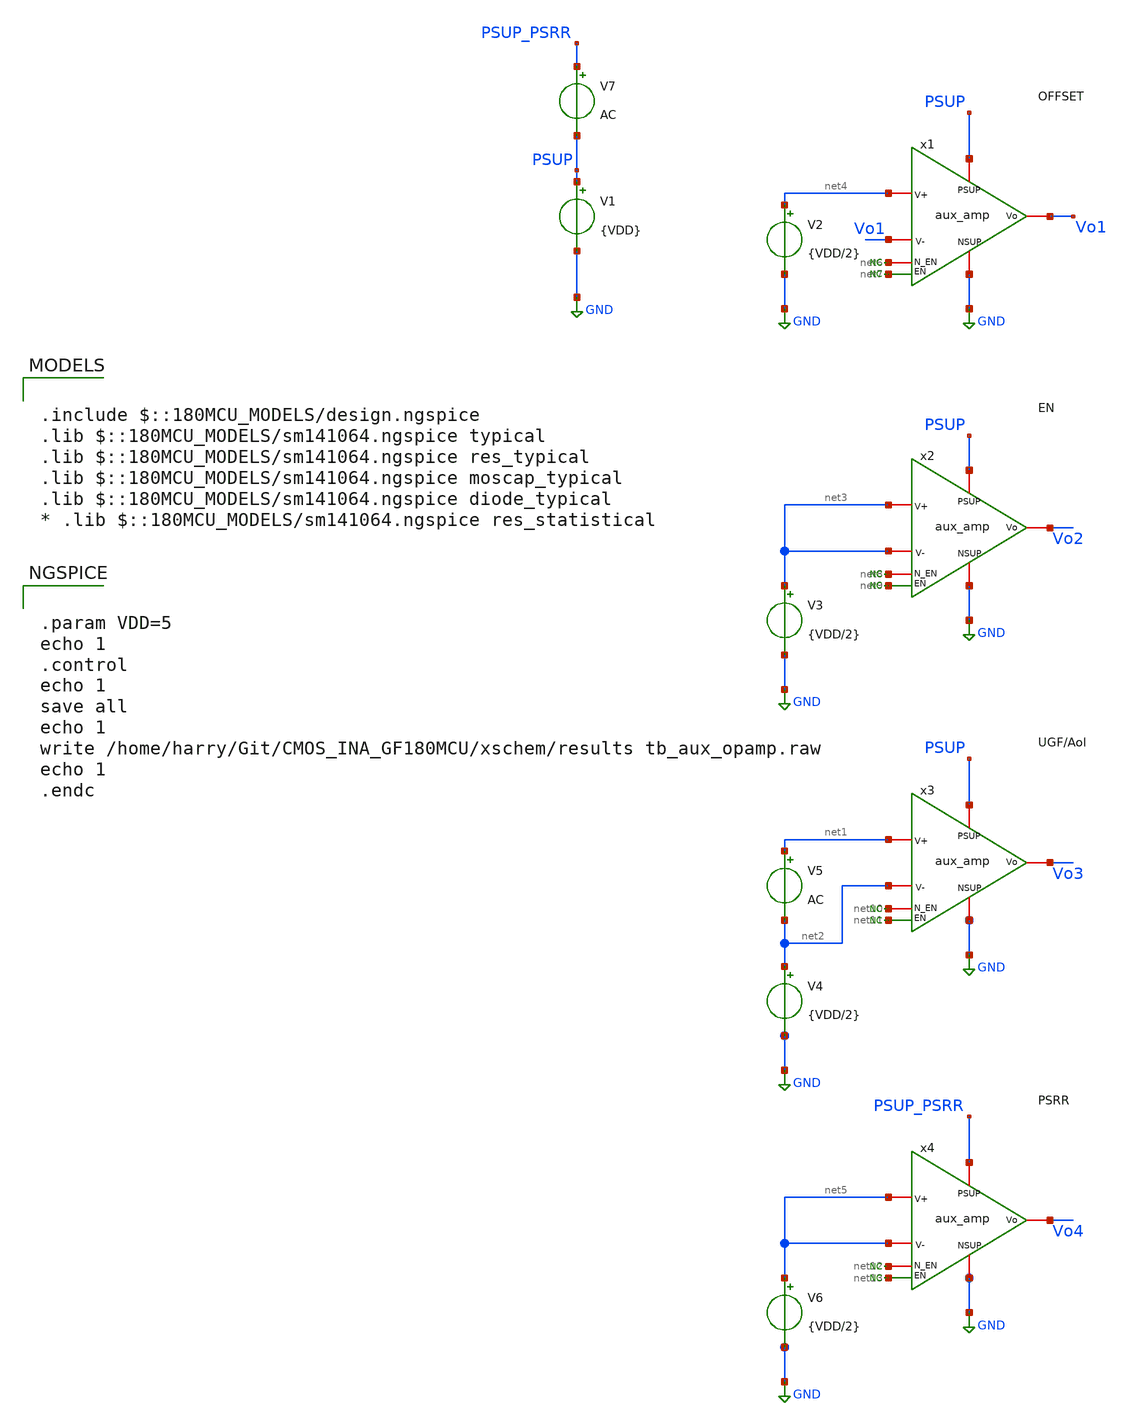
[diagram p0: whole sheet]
** sch_path: xschem/tb/tb_aux_opamp.sch
**.subckt tb_aux_opamp
V1 PSUP GND {VDD}
V2 net4 GND {VDD/2}
V3 net3 GND {VDD/2}
V4 net2 GND {VDD/2}
V5 net1 net2 AC
V6 net5 GND {VDD/2}
V7 PSUP_PSRR PSUP AC
x1 PSUP Vo1 net4 Vo1 net6 GND net7 aux_amp
x2 PSUP Vo2 net3 net3 net8 GND net9 aux_amp
x3 PSUP Vo3 net1 net2 net10 GND net11 aux_amp
x4 PSUP_PSRR Vo4 net5 net5 net12 GND net13 aux_amp
* noconn #net7
* noconn #net9
* noconn #net11
* noconn #net13
* noconn #net6
* noconn #net8
* noconn #net10
* noconn #net12
**** begin user architecture code

.include $::180MCU_MODELS/design.ngspice
.lib $::180MCU_MODELS/sm141064.ngspice typical
.lib $::180MCU_MODELS/sm141064.ngspice res_typical
.lib $::180MCU_MODELS/sm141064.ngspice moscap_typical
.lib $::180MCU_MODELS/sm141064.ngspice diode_typical
* .lib $::180MCU_MODELS/sm141064.ngspice res_statistical



.param VDD=5
echo 1
.control
echo 1
save all
echo 1
write /home/harry/Git/CMOS_INA_GF180MCU/xschem/results tb_aux_opamp.raw
echo 1
.endc


**** end user architecture code
**.ends

* expanding   symbol:  lib/aux_amp.sym # of pins=7
** sym_path: xschem/lib/aux_amp.sym
** sch_path: xschem/lib/aux_amp.sch
.subckt aux_amp PSUP Vo V+ V- N_EN NSUP EN
*.ipin PSUP
*.ipin NSUP
*.ipin N_EN
*.ipin EN
*.ipin V+
*.ipin V-
*.opin Vo
XM1 Vo V- net2 NSUP nfet_06v0 L=0.5u W=2u nf=4 ad='int((nf+1)/2) * W/nf * 0.18u' as='int((nf+2)/2) * W/nf * 0.18u'
+ pd='2*int((nf+1)/2) * (W/nf + 0.18u)' ps='2*int((nf+2)/2) * (W/nf + 0.18u)' nrd='0.18u / W' nrs='0.18u / W'
+ sa=0 sb=0 sd=0 m=4
XM2 net1 V+ net2 NSUP nfet_06v0 L=0.5u W=2u nf=4 ad='int((nf+1)/2) * W/nf * 0.18u' as='int((nf+2)/2) * W/nf * 0.18u'
+ pd='2*int((nf+1)/2) * (W/nf + 0.18u)' ps='2*int((nf+2)/2) * (W/nf + 0.18u)' nrd='0.18u / W' nrs='0.18u / W'
+ sa=0 sb=0 sd=0 m=4
XM5 net1 net1 PSUP PSUP pfet_06v0 L=2u W=2u nf=1 ad='int((nf+1)/2) * W/nf * 0.18u' as='int((nf+2)/2) * W/nf * 0.18u'
+ pd='2*int((nf+1)/2) * (W/nf + 0.18u)' ps='2*int((nf+2)/2) * (W/nf + 0.18u)' nrd='0.18u / W' nrs='0.18u / W'
+ sa=0 sb=0 sd=0 m=1
XM6 Vo net1 PSUP PSUP pfet_06v0 L=2u W=2u nf=1 ad='int((nf+1)/2) * W/nf * 0.18u' as='int((nf+2)/2) * W/nf * 0.18u'
+ pd='2*int((nf+1)/2) * (W/nf + 0.18u)' ps='2*int((nf+2)/2) * (W/nf + 0.18u)' nrd='0.18u / W' nrs='0.18u / W'
+ sa=0 sb=0 sd=0 m=1
I0 net2 NSUP 5u
* noconn N_EN
* noconn EN
.ends

.GLOBAL GND
.end
